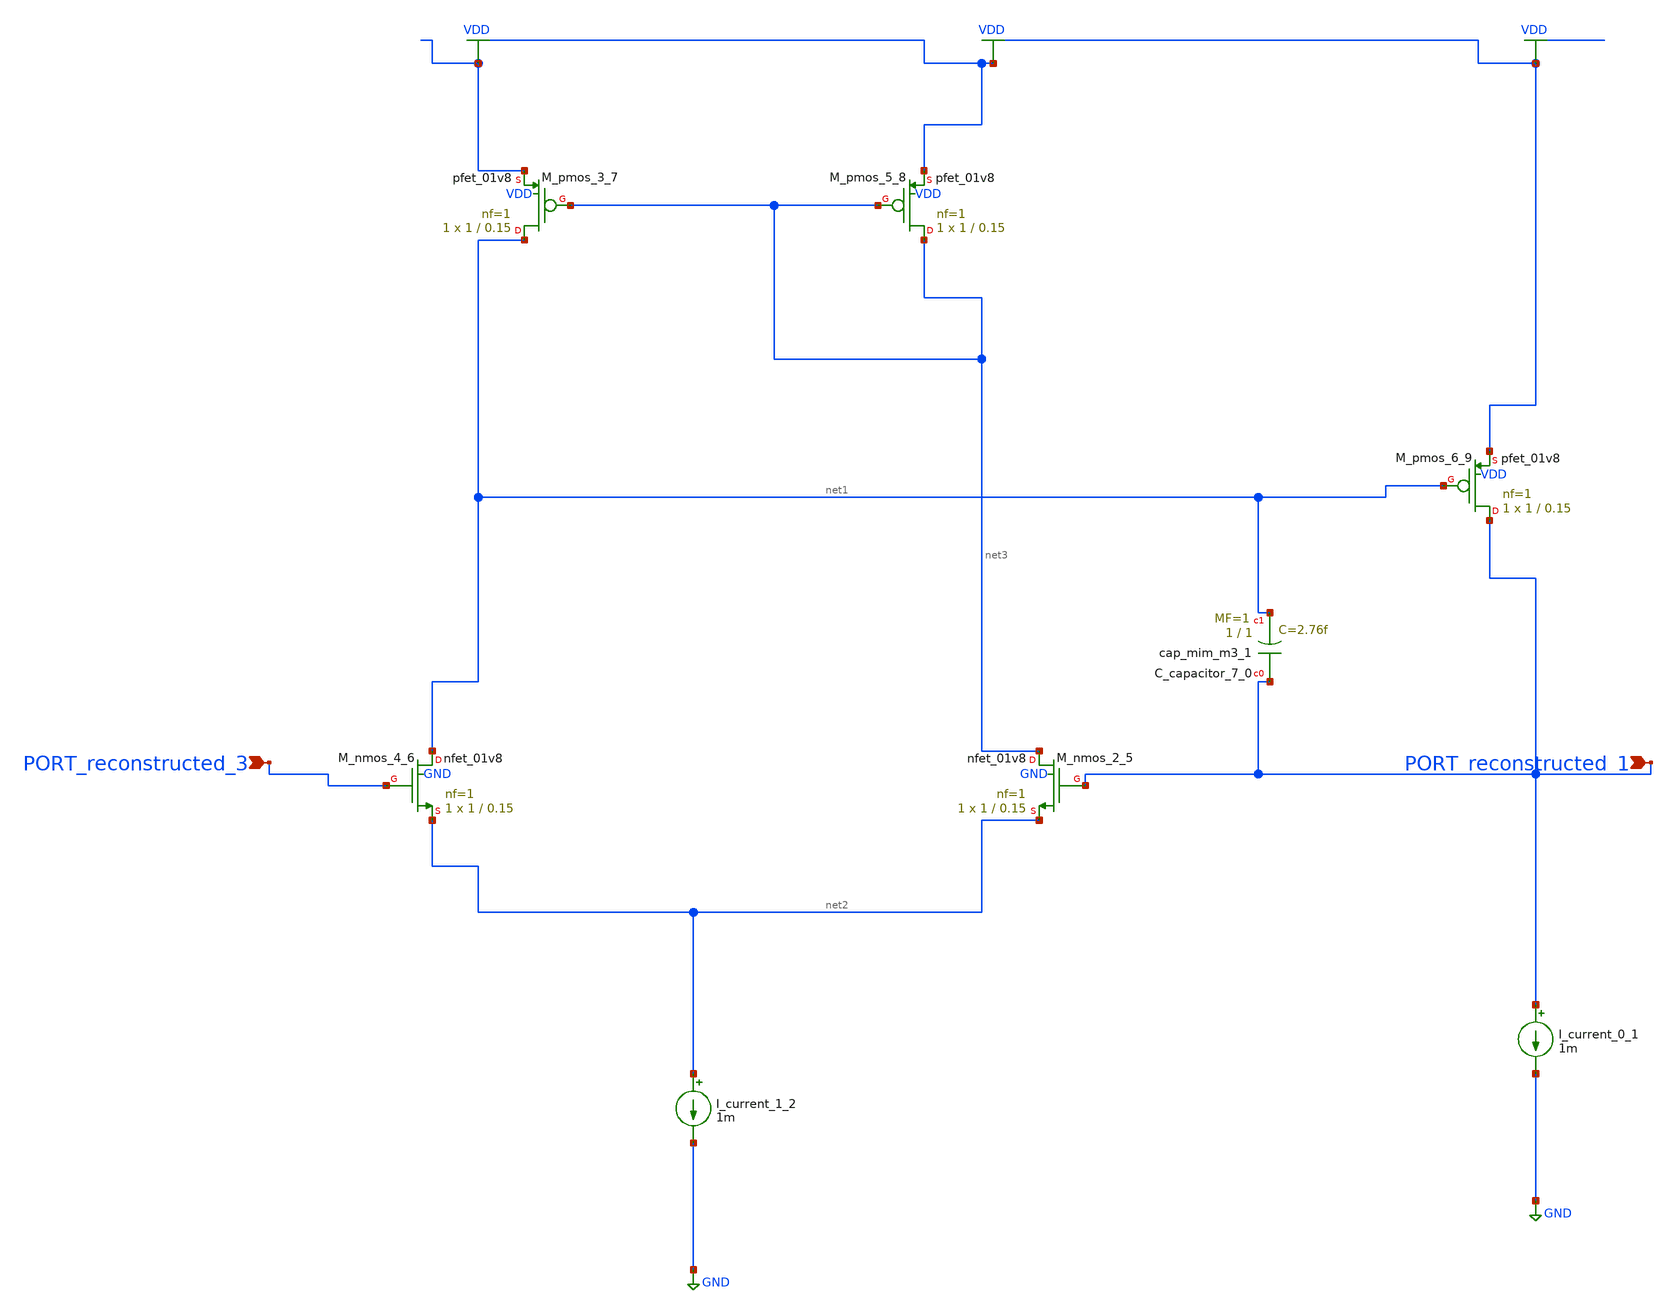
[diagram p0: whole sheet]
** sch_path: schematics/AMSNet/730.sch
**.subckt 730 PORT_reconstructed_1 PORT_reconstructed_3
*.ipin PORT_reconstructed_1
*.ipin PORT_reconstructed_3
XC_capacitor_7_0 PORT_reconstructed_1 net1 sky130_fd_pr__cap_mim_m3_1 W=1 L=1 MF=1 m=1
I_current_0_1 PORT_reconstructed_1 GND 1m
I_current_1_2 net2 GND 1m
XM_nmos_2_5 net3 PORT_reconstructed_1 net2 GND sky130_fd_pr__nfet_01v8 L=0.15 W=1 nf=1 ad='int((1 + 1)/2) * 1 / 1 * 0.29'
+ as='int((1 + 2)/2) * 1 / 1 * 0.29' pd='2*int((1 + 1)/2) * (1 / 1 + 0.29)' ps='2*int((1 + 2)/2) * (1 / 1 + 0.29)'
+ nrd='0.29 / 1 ' nrs='0.29 / 1 ' sa=0 sb=0 sd=0 mult=1 m=1
XM_nmos_4_6 net1 PORT_reconstructed_3 net2 GND sky130_fd_pr__nfet_01v8 L=0.15 W=1 nf=1 ad='int((1 + 1)/2) * 1 / 1 * 0.29'
+ as='int((1 + 2)/2) * 1 / 1 * 0.29' pd='2*int((1 + 1)/2) * (1 / 1 + 0.29)' ps='2*int((1 + 2)/2) * (1 / 1 + 0.29)'
+ nrd='0.29 / 1 ' nrs='0.29 / 1 ' sa=0 sb=0 sd=0 mult=1 m=1
XM_pmos_3_7 net1 net3 VDD VDD sky130_fd_pr__pfet_01v8 L=0.15 W=1 nf=1 ad='int((1 + 1)/2) * 1 / 1 * 0.29'
+ as='int((1 + 2)/2) * 1 / 1 * 0.29' pd='2*int((1 + 1)/2) * (1 / 1 + 0.29)' ps='2*int((1 + 2)/2) * (1 / 1 + 0.29)'
+ nrd='0.29 / 1 ' nrs='0.29 / 1 ' sa=0 sb=0 sd=0 mult=1 m=1
XM_pmos_5_8 net3 net3 VDD VDD sky130_fd_pr__pfet_01v8 L=0.15 W=1 nf=1 ad='int((1 + 1)/2) * 1 / 1 * 0.29'
+ as='int((1 + 2)/2) * 1 / 1 * 0.29' pd='2*int((1 + 1)/2) * (1 / 1 + 0.29)' ps='2*int((1 + 2)/2) * (1 / 1 + 0.29)'
+ nrd='0.29 / 1 ' nrs='0.29 / 1 ' sa=0 sb=0 sd=0 mult=1 m=1
XM_pmos_6_9 PORT_reconstructed_1 net1 VDD VDD sky130_fd_pr__pfet_01v8 L=0.15 W=1 nf=1 ad='int((1 + 1)/2) * 1 / 1 * 0.29'
+ as='int((1 + 2)/2) * 1 / 1 * 0.29' pd='2*int((1 + 1)/2) * (1 / 1 + 0.29)' ps='2*int((1 + 2)/2) * (1 / 1 + 0.29)'
+ nrd='0.29 / 1 ' nrs='0.29 / 1 ' sa=0 sb=0 sd=0 mult=1 m=1
**.ends
.GLOBAL GND
.GLOBAL VDD
.end
